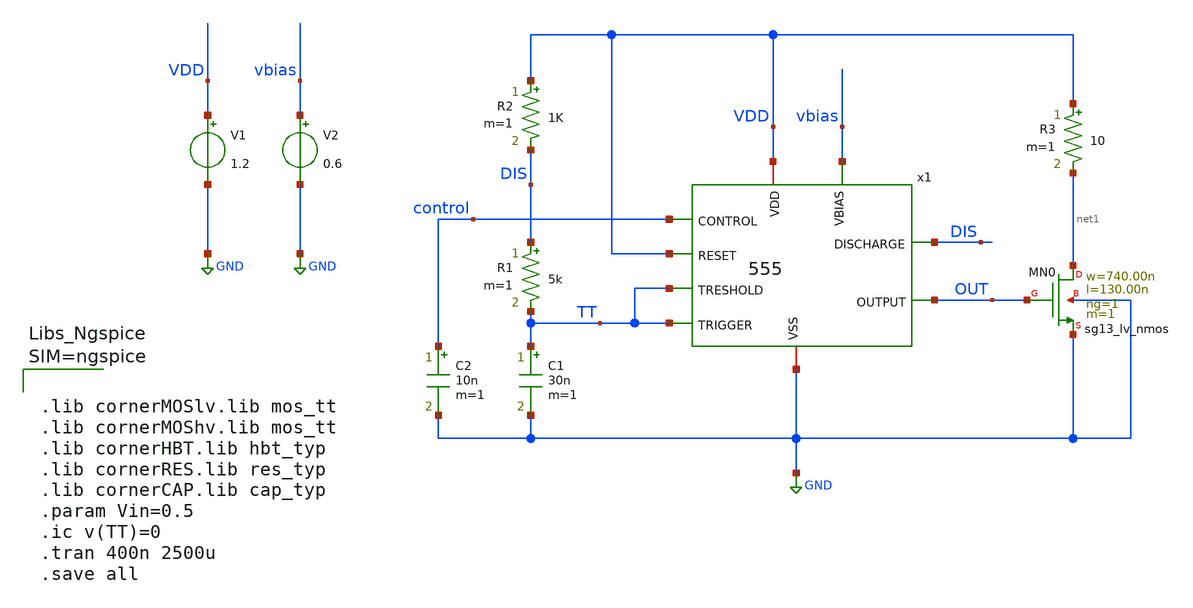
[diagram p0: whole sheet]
** sch_path: schematic/555TB.sch
**.subckt 555TB
x1 VDD TT DIS control vbias VDD OUT TT GND 555
V1 VDD GND 1.2
V2 vbias GND 0.6
R1 DIS TT 5k m=1
C1 TT GND 30n m=1
R2 VDD DIS 1K m=1
C2 control GND 10n m=1
R3 VDD net1 10 m=1
XMN0 net1 OUT GND GND sg13_lv_nmos w=740.00n l=130.00n ng=1 m=1 mm_ok=1
**** begin user architecture code



.lib cornerMOSlv.lib mos_tt
.lib cornerMOShv.lib mos_tt
.lib cornerHBT.lib hbt_typ
.lib cornerRES.lib res_typ
.lib cornerCAP.lib cap_typ
.param Vin=0.5
.ic v(TT)=0
.tran 400n 2500u
.save all



**** end user architecture code
**.ends
.GLOBAL GND
.end
